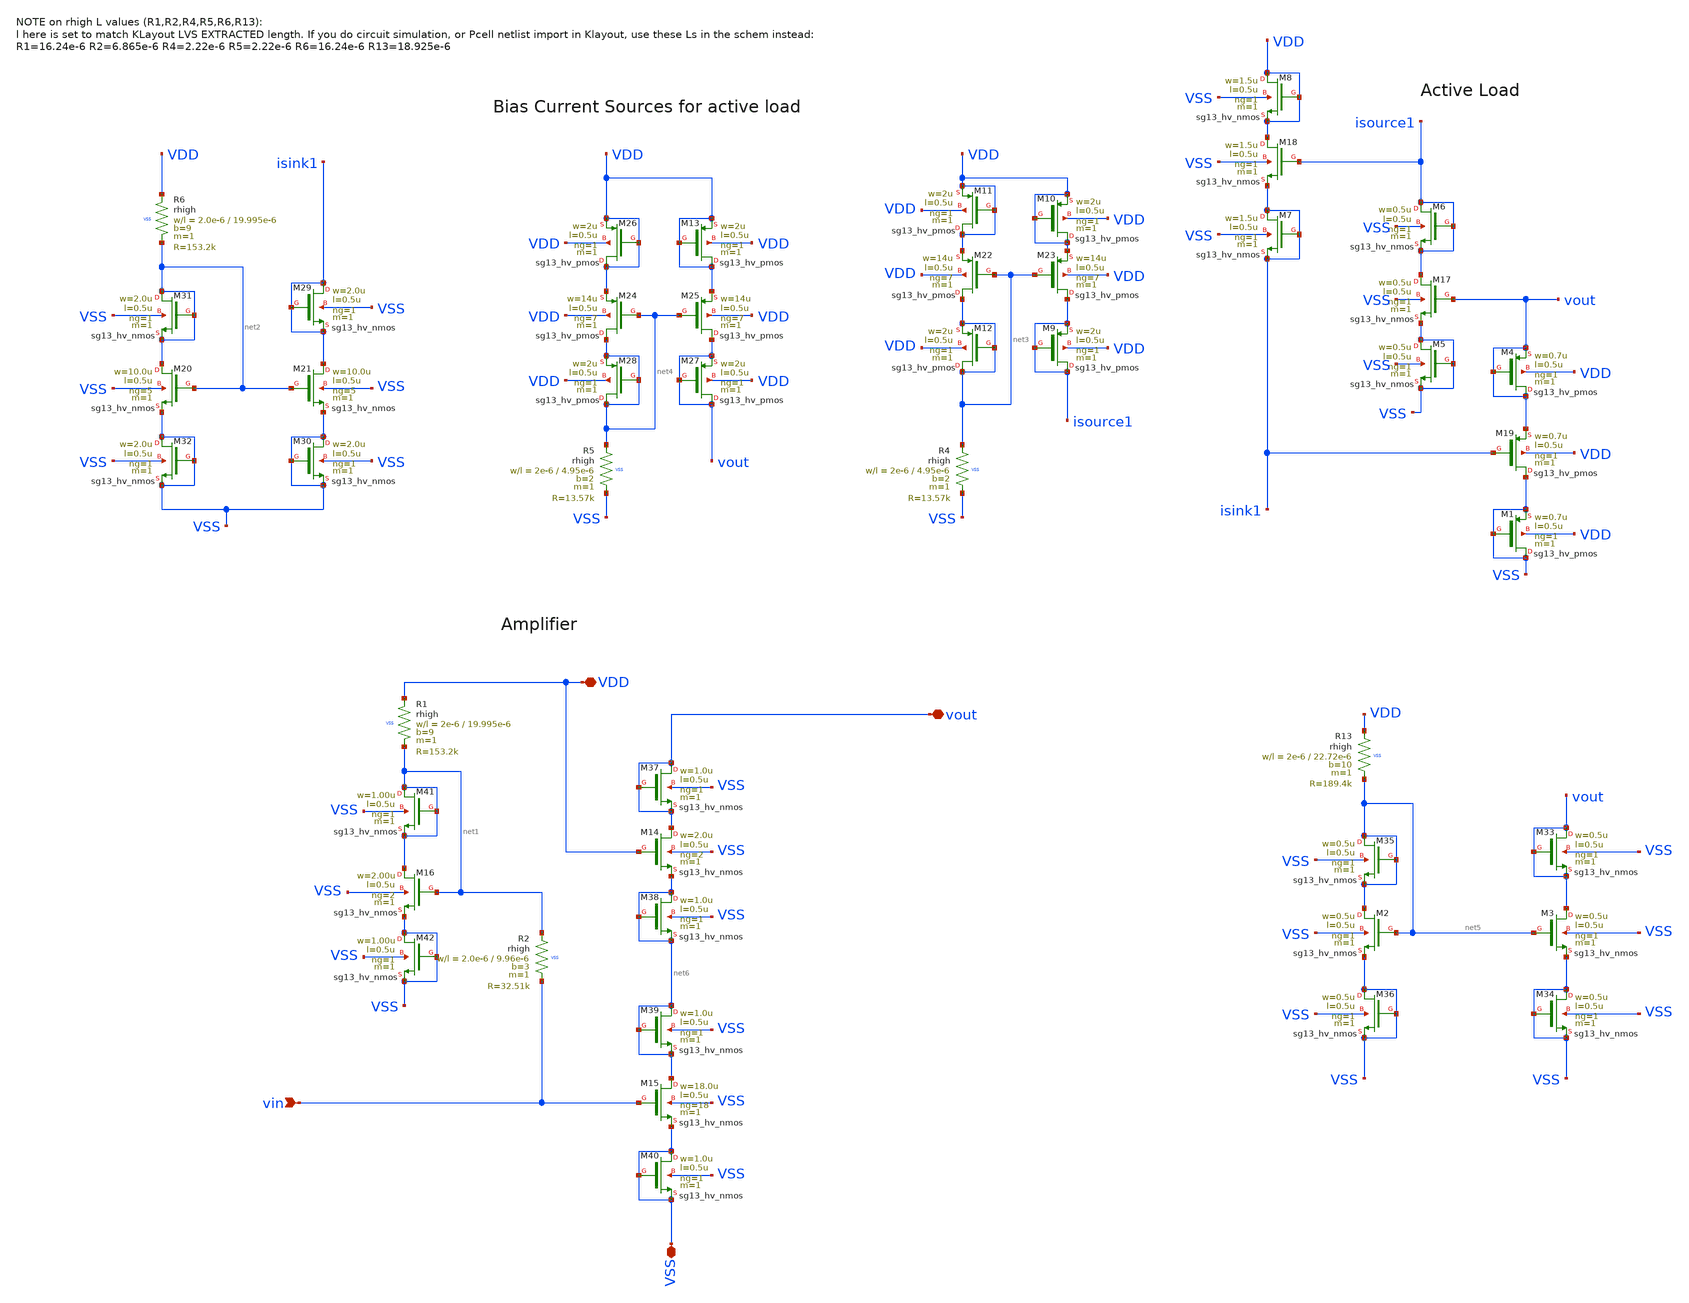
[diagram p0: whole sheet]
** sch_path: macros/heichips26_ook_top/macros/ook_analog_system/schematic/xschem/lna.sch
**.subckt lna VDD VSS vin vout
*.iopin VDD
*.iopin VSS
*.ipin vin
*.iopin vout
XM14 vout VDD net6 VSS sg13_hv_nmos w=2.0u l=0.5u ng=2 m=1 mm_ok=1
XM15 net6 vin VSS VSS sg13_hv_nmos w=18.0u l=0.5u ng=18 m=1 mm_ok=1
XM16 net1 net1 VSS VSS sg13_hv_nmos w=2.00u l=0.5u ng=2 m=1 mm_ok=1
XM17 isource1 vout VSS VSS sg13_hv_nmos w=0.5u l=0.5u ng=1 m=1 mm_ok=1
XM18 VDD isource1 isink1 VSS sg13_hv_nmos w=1.5u l=0.5u ng=1 m=1 mm_ok=1
XM19 VSS isink1 vout VDD sg13_hv_pmos w=0.7u l=0.5u ng=1 m=1 mm_ok=1
XM20 net2 net2 VSS VSS sg13_hv_nmos w=10.0u l=0.5u ng=5 m=1 mm_ok=1
XM21 isink1 net2 VSS VSS sg13_hv_nmos w=10.0u l=0.5u ng=5 m=1 mm_ok=1
XM22 net3 net3 VDD VDD sg13_hv_pmos w=14u l=0.5u ng=7 m=1 mm_ok=1
XM23 isource1 net3 VDD VDD sg13_hv_pmos w=14u l=0.5u ng=7 m=1 mm_ok=1
XM24 net4 net4 VDD VDD sg13_hv_pmos w=14u l=0.5u ng=7 m=1 mm_ok=1
XM25 vout net4 VDD VDD sg13_hv_pmos w=14u l=0.5u ng=7 m=1 mm_ok=1
XR2 net1 vin VSS rhigh w=2.0e-6 l=9.96e-6 m=1 b=3 ps=0.18e-6 mm_ok=1
XR5 net4 VSS VSS rhigh w=2e-6 l=4.95e-6 m=1 b=2 ps=0.18e-6 mm_ok=1
XR1 VDD net1 VSS rhigh w=2e-6 l=19.995e-6 m=1 b=9 ps=0.18e-6 mm_ok=1
XR6 VDD net2 VSS rhigh w=2.0e-6 l=19.995e-6 m=1 b=9 ps=0.18e-6 mm_ok=1
XM2 net5 net5 VSS VSS sg13_hv_nmos w=0.5u l=0.5u ng=1 m=1 mm_ok=1
XM3 vout net5 VSS VSS sg13_hv_nmos w=0.5u l=0.5u ng=1 m=1 mm_ok=1
XR4 net3 VSS VSS rhigh w=2e-6 l=4.95e-6 m=1 b=2 ps=0.18e-6 mm_ok=1
XR13 VDD net5 VSS rhigh w=2e-6 l=22.72e-6 m=1 b=10 ps=0.18e-6 mm_ok=1
XM1 VSS VSS VSS VDD sg13_hv_pmos w=0.7u l=0.5u ng=1 m=1 mm_ok=1
XM4 vout vout vout VDD sg13_hv_pmos w=0.7u l=0.5u ng=1 m=1 mm_ok=1
XM5 VSS VSS VSS VSS sg13_hv_nmos w=0.5u l=0.5u ng=1 m=1 mm_ok=1
XM6 isource1 isource1 isource1 VSS sg13_hv_nmos w=0.5u l=0.5u ng=1 m=1 mm_ok=1
XM7 isink1 isink1 isink1 VSS sg13_hv_nmos w=1.5u l=0.5u ng=1 m=1 mm_ok=1
XM8 VDD VDD VDD VSS sg13_hv_nmos w=1.5u l=0.5u ng=1 m=1 mm_ok=1
XM9 isource1 isource1 isource1 VDD sg13_hv_pmos w=2u l=0.5u ng=1 m=1 mm_ok=1
XM10 VDD VDD VDD VDD sg13_hv_pmos w=2u l=0.5u ng=1 m=1 mm_ok=1
XM11 VDD VDD VDD VDD sg13_hv_pmos w=2u l=0.5u ng=1 m=1 mm_ok=1
XM12 net3 net3 net3 VDD sg13_hv_pmos w=2u l=0.5u ng=1 m=1 mm_ok=1
XM13 VDD VDD VDD VDD sg13_hv_pmos w=2u l=0.5u ng=1 m=1 mm_ok=1
XM26 VDD VDD VDD VDD sg13_hv_pmos w=2u l=0.5u ng=1 m=1 mm_ok=1
XM27 vout vout vout VDD sg13_hv_pmos w=2u l=0.5u ng=1 m=1 mm_ok=1
XM28 net4 net4 net4 VDD sg13_hv_pmos w=2u l=0.5u ng=1 m=1 mm_ok=1
XM29 isink1 isink1 isink1 VSS sg13_hv_nmos w=2.0u l=0.5u ng=1 m=1 mm_ok=1
XM30 VSS VSS VSS VSS sg13_hv_nmos w=2.0u l=0.5u ng=1 m=1 mm_ok=1
XM31 net2 net2 net2 VSS sg13_hv_nmos w=2.0u l=0.5u ng=1 m=1 mm_ok=1
XM32 VSS VSS VSS VSS sg13_hv_nmos w=2.0u l=0.5u ng=1 m=1 mm_ok=1
XM33 vout vout vout VSS sg13_hv_nmos w=0.5u l=0.5u ng=1 m=1 mm_ok=1
XM34 VSS VSS VSS VSS sg13_hv_nmos w=0.5u l=0.5u ng=1 m=1 mm_ok=1
XM35 net5 net5 net5 VSS sg13_hv_nmos w=0.5u l=0.5u ng=1 m=1 mm_ok=1
XM36 VSS VSS VSS VSS sg13_hv_nmos w=0.5u l=0.5u ng=1 m=1 mm_ok=1
XM37 vout vout vout VSS sg13_hv_nmos w=1.0u l=0.5u ng=1 m=1 mm_ok=1
XM38 net6 net6 net6 VSS sg13_hv_nmos w=1.0u l=0.5u ng=1 m=1 mm_ok=1
XM39 net6 net6 net6 VSS sg13_hv_nmos w=1.0u l=0.5u ng=1 m=1 mm_ok=1
XM40 VSS VSS VSS VSS sg13_hv_nmos w=1.0u l=0.5u ng=1 m=1 mm_ok=1
XM41 net1 net1 net1 VSS sg13_hv_nmos w=1.00u l=0.5u ng=1 m=1 mm_ok=1
XM42 VSS VSS VSS VSS sg13_hv_nmos w=1.00u l=0.5u ng=1 m=1 mm_ok=1
**.ends
.end
